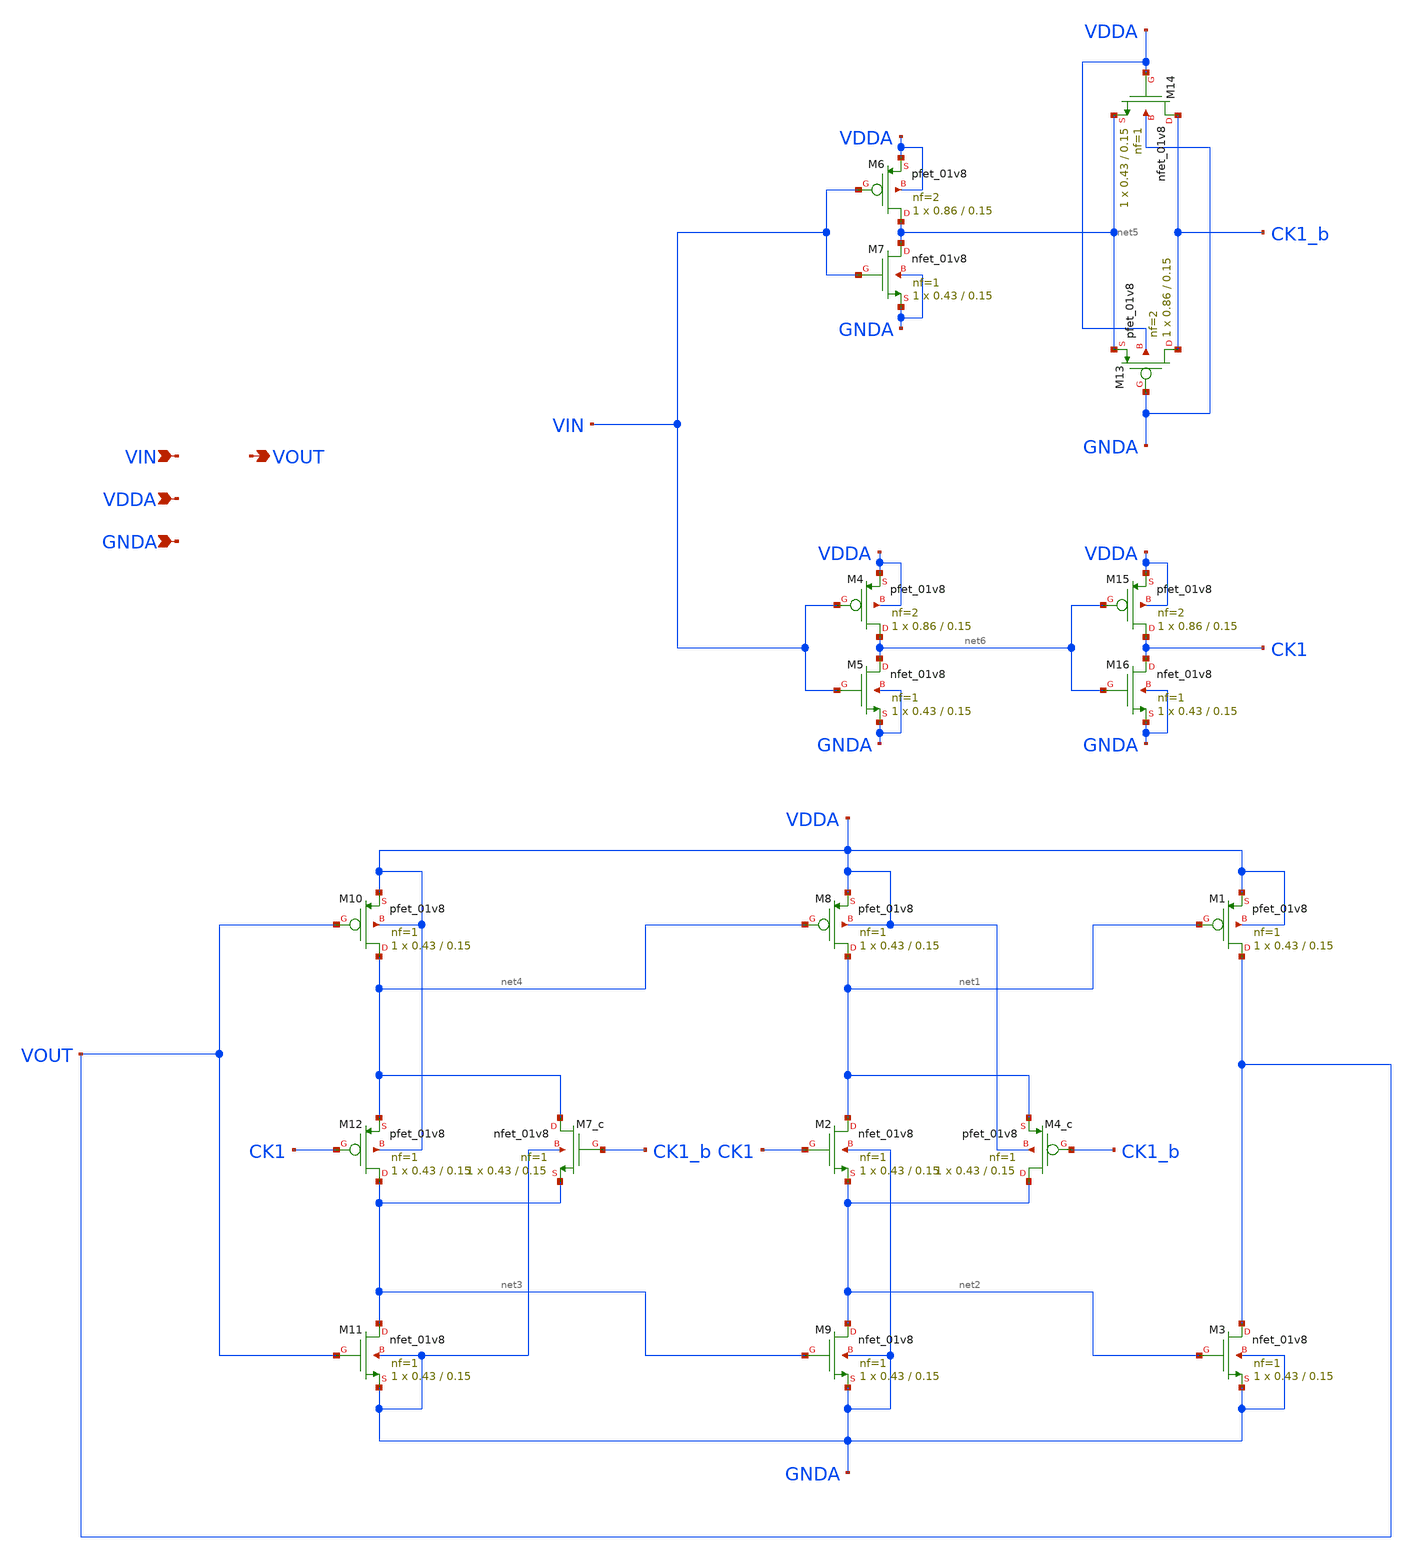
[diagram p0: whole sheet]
** sch_path: projects/pll/divider/xschem_ngspice/TSPC_FF_comp_sw_divide2.sch
**.subckt TSPC_FF_comp_sw_divide2 VIN VOUT VDDA GNDA
*.ipin VIN
*.opin VOUT
*.ipin VDDA
*.ipin GNDA
XM1 VOUT net1 VDDA VDDA sky130_fd_pr__pfet_01v8 L=0.15 W=0.43 nf=1 ad='int((nf+1)/2) * W/nf * 0.29' as='int((nf+2)/2) * W/nf * 0.29'
+ pd='2*int((nf+1)/2) * (W/nf + 0.29)' ps='2*int((nf+2)/2) * (W/nf + 0.29)' nrd='0.29 / W' nrs='0.29 / W'
+ sa=0 sb=0 sd=0 mult=1 m=1
XM2 net1 CK1 net2 GNDA sky130_fd_pr__nfet_01v8 L=0.15 W=0.43 nf=1 ad='int((nf+1)/2) * W/nf * 0.29' as='int((nf+2)/2) * W/nf * 0.29'
+ pd='2*int((nf+1)/2) * (W/nf + 0.29)' ps='2*int((nf+2)/2) * (W/nf + 0.29)' nrd='0.29 / W' nrs='0.29 / W'
+ sa=0 sb=0 sd=0 mult=1 m=1
XM3 VOUT net2 GNDA GNDA sky130_fd_pr__nfet_01v8 L=0.15 W=0.43 nf=1 ad='int((nf+1)/2) * W/nf * 0.29' as='int((nf+2)/2) * W/nf * 0.29'
+ pd='2*int((nf+1)/2) * (W/nf + 0.29)' ps='2*int((nf+2)/2) * (W/nf + 0.29)' nrd='0.29 / W' nrs='0.29 / W'
+ sa=0 sb=0 sd=0 mult=1 m=1
XM8 net1 net4 VDDA VDDA sky130_fd_pr__pfet_01v8 L=0.15 W=0.43 nf=1 ad='int((nf+1)/2) * W/nf * 0.29' as='int((nf+2)/2) * W/nf * 0.29'
+ pd='2*int((nf+1)/2) * (W/nf + 0.29)' ps='2*int((nf+2)/2) * (W/nf + 0.29)' nrd='0.29 / W' nrs='0.29 / W'
+ sa=0 sb=0 sd=0 mult=1 m=1
XM9 net2 net3 GNDA GNDA sky130_fd_pr__nfet_01v8 L=0.15 W=0.43 nf=1 ad='int((nf+1)/2) * W/nf * 0.29' as='int((nf+2)/2) * W/nf * 0.29'
+ pd='2*int((nf+1)/2) * (W/nf + 0.29)' ps='2*int((nf+2)/2) * (W/nf + 0.29)' nrd='0.29 / W' nrs='0.29 / W'
+ sa=0 sb=0 sd=0 mult=1 m=1
XM10 net4 VOUT VDDA VDDA sky130_fd_pr__pfet_01v8 L=0.15 W=0.43 nf=1 ad='int((nf+1)/2) * W/nf * 0.29'
+ as='int((nf+2)/2) * W/nf * 0.29' pd='2*int((nf+1)/2) * (W/nf + 0.29)' ps='2*int((nf+2)/2) * (W/nf + 0.29)'
+ nrd='0.29 / W' nrs='0.29 / W' sa=0 sb=0 sd=0 mult=1 m=1
XM11 net3 VOUT GNDA GNDA sky130_fd_pr__nfet_01v8 L=0.15 W=0.43 nf=1 ad='int((nf+1)/2) * W/nf * 0.29'
+ as='int((nf+2)/2) * W/nf * 0.29' pd='2*int((nf+1)/2) * (W/nf + 0.29)' ps='2*int((nf+2)/2) * (W/nf + 0.29)'
+ nrd='0.29 / W' nrs='0.29 / W' sa=0 sb=0 sd=0 mult=1 m=1
XM12 net3 CK1 net4 VDDA sky130_fd_pr__pfet_01v8 L=0.15 W=0.43 nf=1 ad='int((nf+1)/2) * W/nf * 0.29' as='int((nf+2)/2) * W/nf * 0.29'
+ pd='2*int((nf+1)/2) * (W/nf + 0.29)' ps='2*int((nf+2)/2) * (W/nf + 0.29)' nrd='0.29 / W' nrs='0.29 / W'
+ sa=0 sb=0 sd=0 mult=1 m=1
XM4_c net2 CK1_b net1 VDDA sky130_fd_pr__pfet_01v8 L=0.15 W=0.43 nf=1 ad='int((nf+1)/2) * W/nf * 0.29'
+ as='int((nf+2)/2) * W/nf * 0.29' pd='2*int((nf+1)/2) * (W/nf + 0.29)' ps='2*int((nf+2)/2) * (W/nf + 0.29)'
+ nrd='0.29 / W' nrs='0.29 / W' sa=0 sb=0 sd=0 mult=1 m=1
XM7_c net4 CK1_b net3 GNDA sky130_fd_pr__nfet_01v8 L=0.15 W=0.43 nf=1 ad='int((nf+1)/2) * W/nf * 0.29'
+ as='int((nf+2)/2) * W/nf * 0.29' pd='2*int((nf+1)/2) * (W/nf + 0.29)' ps='2*int((nf+2)/2) * (W/nf + 0.29)'
+ nrd='0.29 / W' nrs='0.29 / W' sa=0 sb=0 sd=0 mult=1 m=1
XM13 CK1_b GNDA net5 VDDA sky130_fd_pr__pfet_01v8 L=0.15 W=0.86 nf=2 ad='int((nf+1)/2) * W/nf * 0.29'
+ as='int((nf+2)/2) * W/nf * 0.29' pd='2*int((nf+1)/2) * (W/nf + 0.29)' ps='2*int((nf+2)/2) * (W/nf + 0.29)'
+ nrd='0.29 / W' nrs='0.29 / W' sa=0 sb=0 sd=0 mult=1 m=1
XM14 CK1_b VDDA net5 GNDA sky130_fd_pr__nfet_01v8 L=0.15 W=0.43 nf=1 ad='int((nf+1)/2) * W/nf * 0.29'
+ as='int((nf+2)/2) * W/nf * 0.29' pd='2*int((nf+1)/2) * (W/nf + 0.29)' ps='2*int((nf+2)/2) * (W/nf + 0.29)'
+ nrd='0.29 / W' nrs='0.29 / W' sa=0 sb=0 sd=0 mult=1 m=1
XM15 CK1 net6 VDDA VDDA sky130_fd_pr__pfet_01v8 L=0.15 W=0.86 nf=2 ad='int((nf+1)/2) * W/nf * 0.29' as='int((nf+2)/2) * W/nf * 0.29'
+ pd='2*int((nf+1)/2) * (W/nf + 0.29)' ps='2*int((nf+2)/2) * (W/nf + 0.29)' nrd='0.29 / W' nrs='0.29 / W'
+ sa=0 sb=0 sd=0 mult=1 m=1
XM16 CK1 net6 GNDA GNDA sky130_fd_pr__nfet_01v8 L=0.15 W=0.43 nf=1 ad='int((nf+1)/2) * W/nf * 0.29' as='int((nf+2)/2) * W/nf * 0.29'
+ pd='2*int((nf+1)/2) * (W/nf + 0.29)' ps='2*int((nf+2)/2) * (W/nf + 0.29)' nrd='0.29 / W' nrs='0.29 / W'
+ sa=0 sb=0 sd=0 mult=1 m=1
XM4 net6 VIN VDDA VDDA sky130_fd_pr__pfet_01v8 L=0.15 W=0.86 nf=2 ad='int((nf+1)/2) * W/nf * 0.29' as='int((nf+2)/2) * W/nf * 0.29'
+ pd='2*int((nf+1)/2) * (W/nf + 0.29)' ps='2*int((nf+2)/2) * (W/nf + 0.29)' nrd='0.29 / W' nrs='0.29 / W'
+ sa=0 sb=0 sd=0 mult=1 m=1
XM5 net6 VIN GNDA GNDA sky130_fd_pr__nfet_01v8 L=0.15 W=0.43 nf=1 ad='int((nf+1)/2) * W/nf * 0.29' as='int((nf+2)/2) * W/nf * 0.29'
+ pd='2*int((nf+1)/2) * (W/nf + 0.29)' ps='2*int((nf+2)/2) * (W/nf + 0.29)' nrd='0.29 / W' nrs='0.29 / W'
+ sa=0 sb=0 sd=0 mult=1 m=1
XM6 net5 VIN VDDA VDDA sky130_fd_pr__pfet_01v8 L=0.15 W=0.86 nf=2 ad='int((nf+1)/2) * W/nf * 0.29' as='int((nf+2)/2) * W/nf * 0.29'
+ pd='2*int((nf+1)/2) * (W/nf + 0.29)' ps='2*int((nf+2)/2) * (W/nf + 0.29)' nrd='0.29 / W' nrs='0.29 / W'
+ sa=0 sb=0 sd=0 mult=1 m=1
XM7 net5 VIN GNDA GNDA sky130_fd_pr__nfet_01v8 L=0.15 W=0.43 nf=1 ad='int((nf+1)/2) * W/nf * 0.29' as='int((nf+2)/2) * W/nf * 0.29'
+ pd='2*int((nf+1)/2) * (W/nf + 0.29)' ps='2*int((nf+2)/2) * (W/nf + 0.29)' nrd='0.29 / W' nrs='0.29 / W'
+ sa=0 sb=0 sd=0 mult=1 m=1
**.ends
.end
